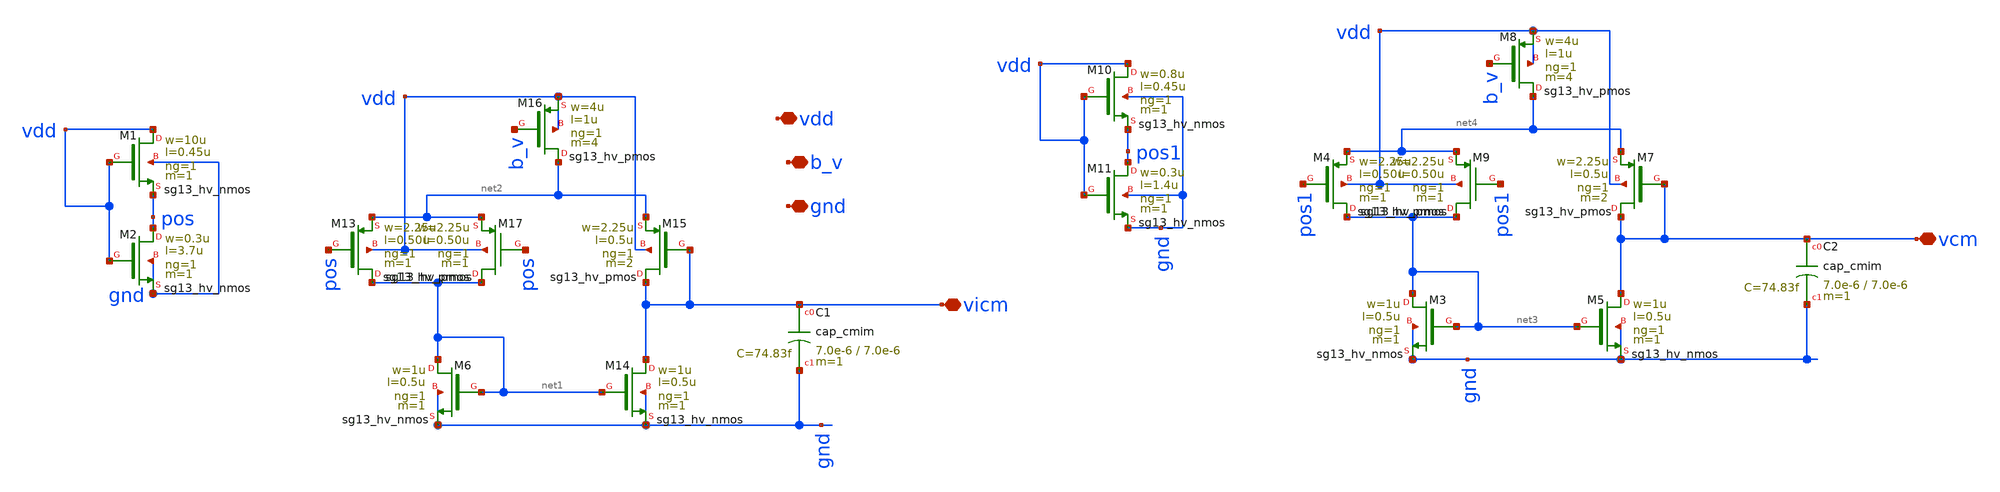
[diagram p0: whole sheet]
** sch_path: dependencies/OTA/dependencies/OTA5174-main/schematic/xschem/vcm_ref_vicm_ref_gen.sch
**.subckt vcm_ref_vicm_ref_gen vicm vdd vcm b_v gnd
*.iopin vicm
*.iopin vdd
*.iopin vcm
*.iopin b_v
*.iopin gnd
XM6 net1 net1 gnd gnd sg13_hv_nmos w=1u l=0.5u ng=1 m=1 mm_ok=1
XM13 net1 pos net2 vdd sg13_hv_pmos w=2.25u l=0.50u ng=1 m=1 mm_ok=1
XM14 vicm net1 gnd gnd sg13_hv_nmos w=1u l=0.5u ng=1 m=1 mm_ok=1
XM15 vicm vicm net2 vdd sg13_hv_pmos w=2.25u l=0.5u ng=1 m=2 mm_ok=1
XM16 net2 b_v vdd vdd sg13_hv_pmos w=4u l=1u ng=1 m=4 mm_ok=1
XM17 net1 pos net2 vdd sg13_hv_pmos w=2.25u l=0.50u ng=1 m=1 mm_ok=1
XM1 vdd vdd pos gnd sg13_hv_nmos w=10u l=0.45u ng=1 m=1 mm_ok=1
XM2 pos vdd gnd gnd sg13_hv_nmos w=0.3u l=3.7u ng=1 m=1 mm_ok=1
XM3 net3 net3 gnd gnd sg13_hv_nmos w=1u l=0.5u ng=1 m=1 mm_ok=1
XM4 net3 pos1 net4 vdd sg13_hv_pmos w=2.25u l=0.50u ng=1 m=1 mm_ok=1
XM5 vcm net3 gnd gnd sg13_hv_nmos w=1u l=0.5u ng=1 m=1 mm_ok=1
XM7 vcm vcm net4 vdd sg13_hv_pmos w=2.25u l=0.5u ng=1 m=2 mm_ok=1
XM8 net4 b_v vdd vdd sg13_hv_pmos w=4u l=1u ng=1 m=4 mm_ok=1
XM9 net3 pos1 net4 vdd sg13_hv_pmos w=2.25u l=0.50u ng=1 m=1 mm_ok=1
XM10 vdd vdd pos1 gnd sg13_hv_nmos w=0.8u l=0.45u ng=1 m=1 mm_ok=1
XM11 pos1 vdd gnd gnd sg13_hv_nmos w=0.3u l=1.4u ng=1 m=1 mm_ok=1
XC1 vicm gnd cap_cmim w=7.0e-6 l=7.0e-6 m=1 mm_ok=1
XC2 vcm gnd cap_cmim w=7.0e-6 l=7.0e-6 m=1 mm_ok=1
**.ends
.end
